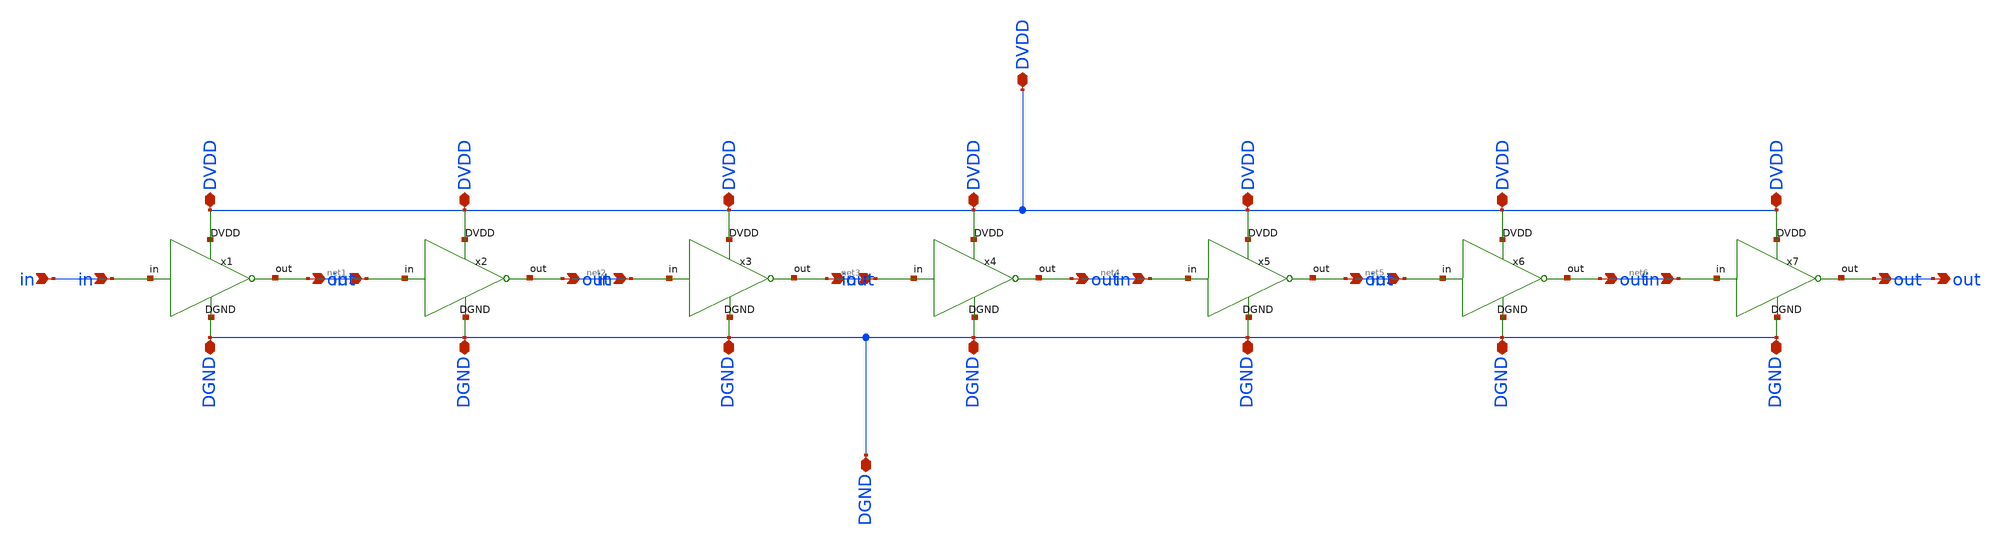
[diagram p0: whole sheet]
** sch_path: assignments/assignment4/ro7.sch
**.subckt ro7 in out DVDD DGND
*.ipin in
*.opin out
*.iopin DVDD
*.iopin DGND
x1 DVDD in net1 DGND inv
x2 DVDD net1 net2 DGND inv
x3 DVDD net2 net3 DGND inv
x4 DVDD net3 net4 DGND inv
x5 DVDD net4 net5 DGND inv
x6 DVDD net5 net6 DGND inv
x7 DVDD net6 out DGND inv
**.ends

* expanding   symbol:  inv.sym # of pins=8
** sym_path: assignments/assignment4/inv.sym
** sch_path: assignments/assignment4/inv.sch
.subckt inv DVDD in out DGND
*.ipin in
*.opin out
*.iopin DVDD
*.iopin DGND
XM3 out in DVDD DVDD sky130_fd_pr__pfet_01v8 L=0.15 W=0.84 nf=1 ad='int((nf+1)/2) * W/nf * 0.29' as='int((nf+2)/2) * W/nf * 0.29'
+ pd='2*int((nf+1)/2) * (W/nf + 0.29)' ps='2*int((nf+2)/2) * (W/nf + 0.29)' nrd='0.29 / W' nrs='0.29 / W'
+ sa=0 sb=0 sd=0 mult=1 m=1
XM2 out in DGND DGND sky130_fd_pr__nfet_01v8 L=0.15 W=0.42 nf=1 ad='int((nf+1)/2) * W/nf * 0.29' as='int((nf+2)/2) * W/nf * 0.29'
+ pd='2*int((nf+1)/2) * (W/nf + 0.29)' ps='2*int((nf+2)/2) * (W/nf + 0.29)' nrd='0.29 / W' nrs='0.29 / W'
+ sa=0 sb=0 sd=0 mult=1 m=1
.ends

.end
